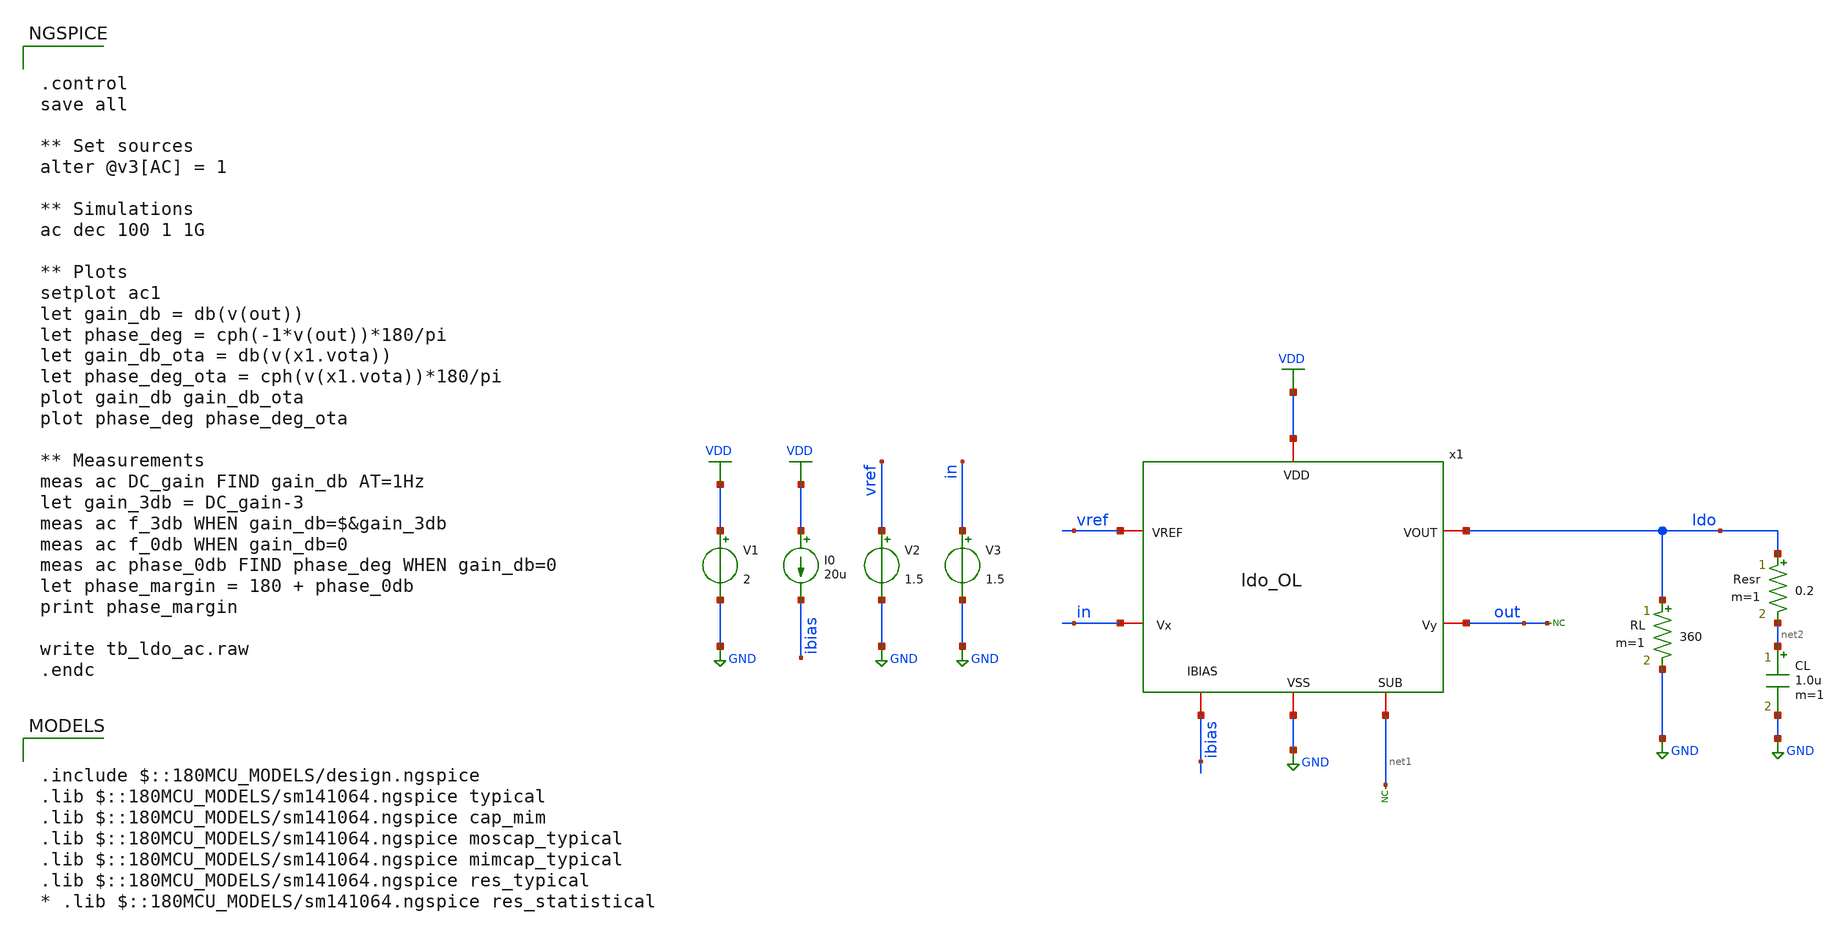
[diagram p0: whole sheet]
** sch_path: designs/libs/tb_ldo/tb_ldo/tb_ldo/tb_ldo_ac/tb_ldo_ac.sch
**.subckt tb_ldo_ac
* noconn #net1
RL ldo GND 360 m=1
V1 VDD GND 2
V2 vref GND 1.5
I0 VDD ibias 20u
CL net2 GND 1.0u m=1
Resr ldo net2 0.2 m=1
x1 VDD vref ldo ibias in out net1 GND ldo_OL
V3 in GND 1.5
* noconn out
**** begin user architecture code

.include $::180MCU_MODELS/design.ngspice
.lib $::180MCU_MODELS/sm141064.ngspice typical
.lib $::180MCU_MODELS/sm141064.ngspice cap_mim
.lib $::180MCU_MODELS/sm141064.ngspice moscap_typical
.lib $::180MCU_MODELS/sm141064.ngspice mimcap_typical
.lib $::180MCU_MODELS/sm141064.ngspice res_typical
* .lib $::180MCU_MODELS/sm141064.ngspice res_statistical



.control
save all

** Set sources
alter @v3[AC] = 1

** Simulations
ac dec 100 1 1G

** Plots
setplot ac1
let gain_db = db(v(out))
let phase_deg = cph(-1*v(out))*180/pi
let gain_db_ota = db(v(x1.vota))
let phase_deg_ota = cph(v(x1.vota))*180/pi
plot gain_db gain_db_ota
plot phase_deg phase_deg_ota

** Measurements
meas ac DC_gain FIND gain_db AT=1Hz
let gain_3db = DC_gain-3
meas ac f_3db WHEN gain_db=$&gain_3db
meas ac f_0db WHEN gain_db=0
meas ac phase_0db FIND phase_deg WHEN gain_db=0
let phase_margin = 180 + phase_0db
print phase_margin

write tb_ldo_ac.raw
.endc


**** end user architecture code
**.ends

* expanding   symbol:  libs/core_ldo/ldo/ldo_ldo_OL/ldo_OL.sym # of pins=8
** sym_path: designs/libs/core_ldo/ldo/ldo_ldo_OL/ldo_OL.sym
** sch_path: designs/libs/core_ldo/ldo/ldo_ldo_OL/ldo_OL.sch
.subckt ldo_OL VDD VREF VOUT IBIAS Vx Vy SUB VSS
*.iopin VDD
*.iopin VSS
*.iopin VOUT
*.iopin SUB
*.iopin VREF
*.iopin IBIAS
*.iopin Vx
*.iopin Vy
XM11 VOUT Vota VDD VDD pfet_05v0 L=0.50u W=100.00u nf=1 ad='int((nf+1)/2) * W/nf * 0.18u' as='int((nf+2)/2) * W/nf * 0.18u'
+ pd='2*int((nf+1)/2) * (W/nf + 0.18u)' ps='2*int((nf+2)/2) * (W/nf + 0.18u)' nrd='0.18u / W' nrs='0.18u / W'
+ sa=0 sb=0 sd=0 m=5
* noconn SUB
x1 VDD VREF Vx Vota IBIAS VSS OTA
XR1 Vy VOUT VDD ppolyf_u_1k r_width=1e-6 r_length=10e-6 m=1
XR2 VSS Vy VDD ppolyf_u_1k r_width=1e-6 r_length=50e-6 m=1
XRc VOUT net1 VDD ppolyf_u_1k r_width=1e-6 r_length=1e-6 m=1
XCc Vota net1 cap_mim_1f0fF c_width=10e-6 c_length=10e-6 m=10
.ends


* expanding   symbol:  libs/core_ldo/ldo/ldo_OTA/OTA.sym # of pins=6
** sym_path: designs/libs/core_ldo/ldo/OTA.sym
** sch_path: designs/libs/core_ldo/ldo/OTA.sch
.subckt OTA VDD VREF VFB VOTA IBIAS VSS
*.iopin VDD
*.iopin VSS
*.iopin VOTA
*.iopin VREF
*.iopin IBIAS
*.iopin VFB
XM3 net2 net2 VDD VDD pfet_05v0 L=2.00u W=8.00u nf=1 ad='int((nf+1)/2) * W/nf * 0.18u' as='int((nf+2)/2) * W/nf * 0.18u'
+ pd='2*int((nf+1)/2) * (W/nf + 0.18u)' ps='2*int((nf+2)/2) * (W/nf + 0.18u)' nrd='0.18u / W' nrs='0.18u / W'
+ sa=0 sb=0 sd=0 m=1
XM4 net3 net3 VDD VDD pfet_05v0 L=2.00u W=8.00u nf=1 ad='int((nf+1)/2) * W/nf * 0.18u' as='int((nf+2)/2) * W/nf * 0.18u'
+ pd='2*int((nf+1)/2) * (W/nf + 0.18u)' ps='2*int((nf+2)/2) * (W/nf + 0.18u)' nrd='0.18u / W' nrs='0.18u / W'
+ sa=0 sb=0 sd=0 m=1
XM5 net4 net2 VDD VDD pfet_05v0 L=2.00u W=8.00u nf=1 ad='int((nf+1)/2) * W/nf * 0.18u' as='int((nf+2)/2) * W/nf * 0.18u'
+ pd='2*int((nf+1)/2) * (W/nf + 0.18u)' ps='2*int((nf+2)/2) * (W/nf + 0.18u)' nrd='0.18u / W' nrs='0.18u / W'
+ sa=0 sb=0 sd=0 m=1
XM6 VOTA net3 VDD VDD pfet_05v0 L=2.00u W=8.00u nf=1 ad='int((nf+1)/2) * W/nf * 0.18u' as='int((nf+2)/2) * W/nf * 0.18u'
+ pd='2*int((nf+1)/2) * (W/nf + 0.18u)' ps='2*int((nf+2)/2) * (W/nf + 0.18u)' nrd='0.18u / W' nrs='0.18u / W'
+ sa=0 sb=0 sd=0 m=2
XM9 IBIAS IBIAS VSS VSS nfet_05v0 L=2.00u W=4.00u nf=1 ad='int((nf+1)/2) * W/nf * 0.18u' as='int((nf+2)/2) * W/nf * 0.18u'
+ pd='2*int((nf+1)/2) * (W/nf + 0.18u)' ps='2*int((nf+2)/2) * (W/nf + 0.18u)' nrd='0.18u / W' nrs='0.18u / W'
+ sa=0 sb=0 sd=0 m=1
XM10 net1 IBIAS VSS VSS nfet_05v0 L=2.00u W=4.00u nf=1 ad='int((nf+1)/2) * W/nf * 0.18u' as='int((nf+2)/2) * W/nf * 0.18u'
+ pd='2*int((nf+1)/2) * (W/nf + 0.18u)' ps='2*int((nf+2)/2) * (W/nf + 0.18u)' nrd='0.18u / W' nrs='0.18u / W'
+ sa=0 sb=0 sd=0 m=1
XM7 net4 net4 VSS VSS nfet_05v0 L=2.00u W=4.00u nf=1 ad='int((nf+1)/2) * W/nf * 0.18u' as='int((nf+2)/2) * W/nf * 0.18u'
+ pd='2*int((nf+1)/2) * (W/nf + 0.18u)' ps='2*int((nf+2)/2) * (W/nf + 0.18u)' nrd='0.18u / W' nrs='0.18u / W'
+ sa=0 sb=0 sd=0 m=1
XM8 VOTA net4 VSS VSS nfet_05v0 L=2.00u W=4.00u nf=1 ad='int((nf+1)/2) * W/nf * 0.18u' as='int((nf+2)/2) * W/nf * 0.18u'
+ pd='2*int((nf+1)/2) * (W/nf + 0.18u)' ps='2*int((nf+2)/2) * (W/nf + 0.18u)' nrd='0.18u / W' nrs='0.18u / W'
+ sa=0 sb=0 sd=0 m=2
XM1 net2 VREF net1 net1 nfet_05v0 L=0.60u W=40.00u nf=1 ad='int((nf+1)/2) * W/nf * 0.18u' as='int((nf+2)/2) * W/nf * 0.18u'
+ pd='2*int((nf+1)/2) * (W/nf + 0.18u)' ps='2*int((nf+2)/2) * (W/nf + 0.18u)' nrd='0.18u / W' nrs='0.18u / W'
+ sa=0 sb=0 sd=0 m=1
XM2 net3 VFB net1 net1 nfet_05v0 L=0.60u W=40.00u nf=1 ad='int((nf+1)/2) * W/nf * 0.18u' as='int((nf+2)/2) * W/nf * 0.18u'
+ pd='2*int((nf+1)/2) * (W/nf + 0.18u)' ps='2*int((nf+2)/2) * (W/nf + 0.18u)' nrd='0.18u / W' nrs='0.18u / W'
+ sa=0 sb=0 sd=0 m=1
.ends

.GLOBAL GND
.GLOBAL VDD
.end
